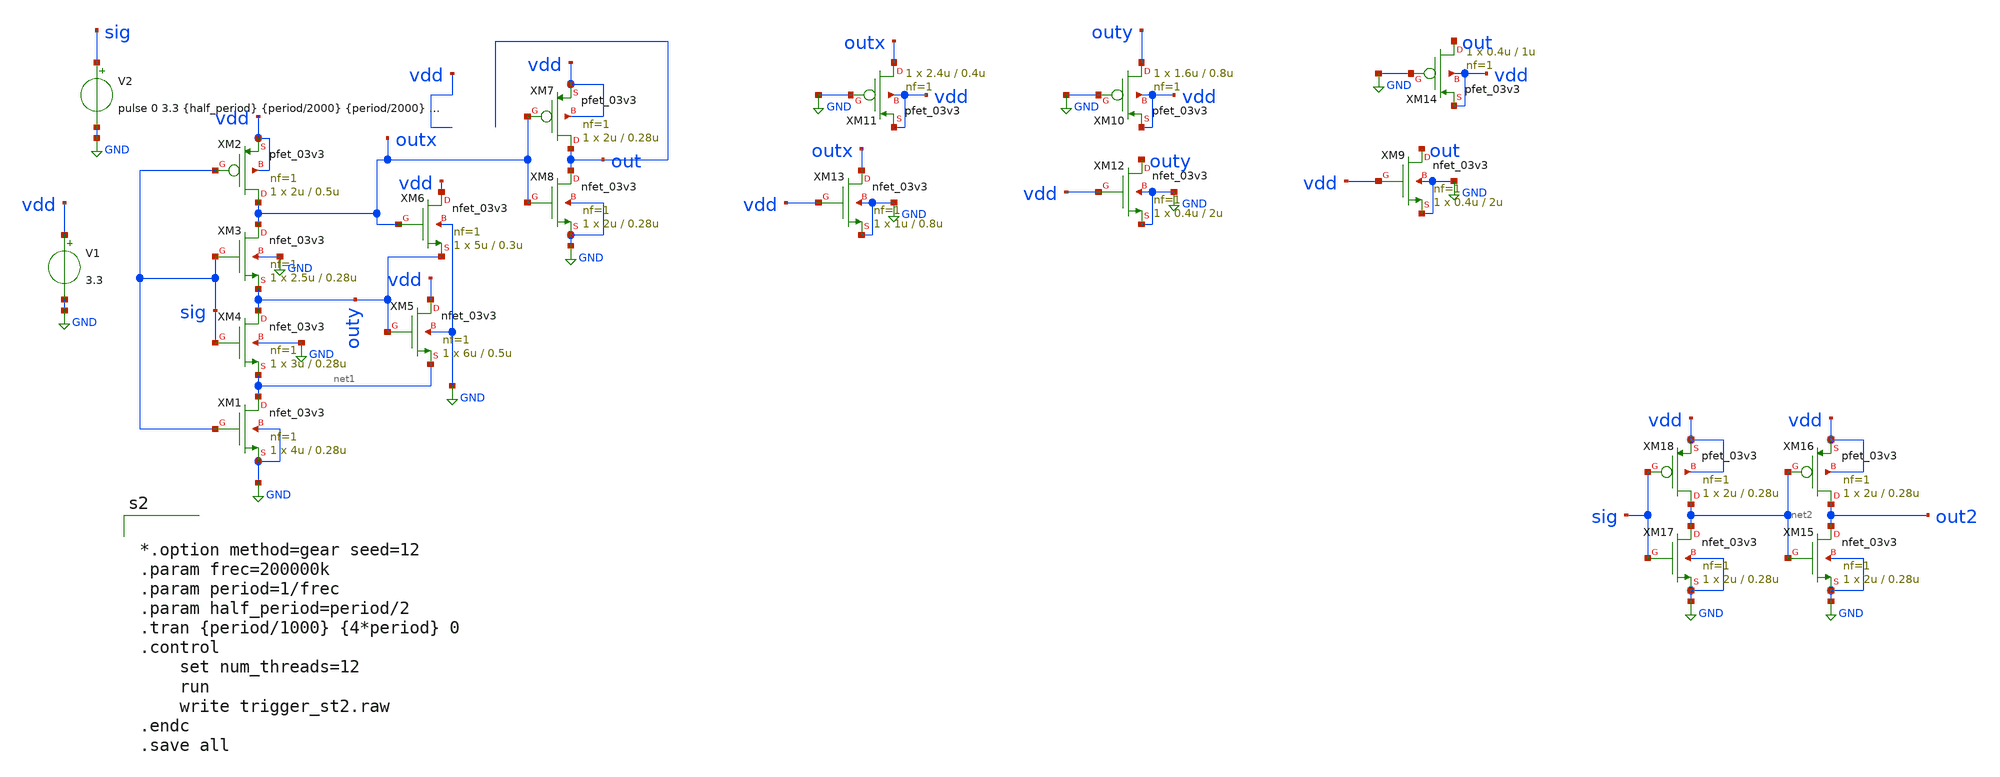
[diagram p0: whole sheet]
** sch_path: designs/libs/tb_trigger/trigger_st2.sch
**.subckt trigger_st2
XM2 outx sig vdd vdd pfet_03v3 L=0.5u W=2u nf=1 ad='int((nf+1)/2) * W/nf * 0.18u' as='int((nf+2)/2) * W/nf * 0.18u'
+ pd='2*int((nf+1)/2) * (W/nf + 0.18u)' ps='2*int((nf+2)/2) * (W/nf + 0.18u)' nrd='0.18u / W' nrs='0.18u / W'
+ sa=0 sb=0 sd=0 m=1
V2 sig GND pulse 0 3.3 {half_period} {period/2000} {period/2000} {half_period} {period}
V1 vdd GND 3.3
XM1 net1 sig GND GND nfet_03v3 L=0.28u W=4u nf=1 ad='int((nf+1)/2) * W/nf * 0.18u' as='int((nf+2)/2) * W/nf * 0.18u'
+ pd='2*int((nf+1)/2) * (W/nf + 0.18u)' ps='2*int((nf+2)/2) * (W/nf + 0.18u)' nrd='0.18u / W' nrs='0.18u / W'
+ sa=0 sb=0 sd=0 m=1
XM4 outy sig net1 GND nfet_03v3 L=0.28u W=3u nf=1 ad='int((nf+1)/2) * W/nf * 0.18u' as='int((nf+2)/2) * W/nf * 0.18u'
+ pd='2*int((nf+1)/2) * (W/nf + 0.18u)' ps='2*int((nf+2)/2) * (W/nf + 0.18u)' nrd='0.18u / W' nrs='0.18u / W'
+ sa=0 sb=0 sd=0 m=1
XM3 outx sig outy GND nfet_03v3 L=0.28u W=2.5u nf=1 ad='int((nf+1)/2) * W/nf * 0.18u' as='int((nf+2)/2) * W/nf * 0.18u'
+ pd='2*int((nf+1)/2) * (W/nf + 0.18u)' ps='2*int((nf+2)/2) * (W/nf + 0.18u)' nrd='0.18u / W' nrs='0.18u / W'
+ sa=0 sb=0 sd=0 m=1
XM5 vdd outy net1 GND nfet_03v3 L=0.5u W=6u nf=1 ad='int((nf+1)/2) * W/nf * 0.18u' as='int((nf+2)/2) * W/nf * 0.18u'
+ pd='2*int((nf+1)/2) * (W/nf + 0.18u)' ps='2*int((nf+2)/2) * (W/nf + 0.18u)' nrd='0.18u / W' nrs='0.18u / W'
+ sa=0 sb=0 sd=0 m=1
XM6 vdd outx outy GND nfet_03v3 L=0.3u W=5u nf=1 ad='int((nf+1)/2) * W/nf * 0.18u' as='int((nf+2)/2) * W/nf * 0.18u'
+ pd='2*int((nf+1)/2) * (W/nf + 0.18u)' ps='2*int((nf+2)/2) * (W/nf + 0.18u)' nrd='0.18u / W' nrs='0.18u / W'
+ sa=0 sb=0 sd=0 m=1
XM8 out outx GND GND nfet_03v3 L=0.28u W=2u nf=1 ad='int((nf+1)/2) * W/nf * 0.18u' as='int((nf+2)/2) * W/nf * 0.18u'
+ pd='2*int((nf+1)/2) * (W/nf + 0.18u)' ps='2*int((nf+2)/2) * (W/nf + 0.18u)' nrd='0.18u / W' nrs='0.18u / W'
+ sa=0 sb=0 sd=0 m=1
XM7 out outx vdd vdd pfet_03v3 L=0.28u W=2u nf=1 ad='int((nf+1)/2) * W/nf * 0.18u' as='int((nf+2)/2) * W/nf * 0.18u'
+ pd='2*int((nf+1)/2) * (W/nf + 0.18u)' ps='2*int((nf+2)/2) * (W/nf + 0.18u)' nrd='0.18u / W' nrs='0.18u / W'
+ sa=0 sb=0 sd=0 m=1
XM9 out vdd GND GND nfet_03v3 L=2u W=0.4u nf=1 ad='int((nf+1)/2) * W/nf * 0.18u' as='int((nf+2)/2) * W/nf * 0.18u'
+ pd='2*int((nf+1)/2) * (W/nf + 0.18u)' ps='2*int((nf+2)/2) * (W/nf + 0.18u)' nrd='0.18u / W' nrs='0.18u / W'
+ sa=0 sb=0 sd=0 m=1
XM14 out GND vdd vdd pfet_03v3 L=1u W=0.4u nf=1 ad='int((nf+1)/2) * W/nf * 0.18u' as='int((nf+2)/2) * W/nf * 0.18u'
+ pd='2*int((nf+1)/2) * (W/nf + 0.18u)' ps='2*int((nf+2)/2) * (W/nf + 0.18u)' nrd='0.18u / W' nrs='0.18u / W'
+ sa=0 sb=0 sd=0 m=1
XM10 outy GND vdd vdd pfet_03v3 L=0.8u W=1.6u nf=1 ad='int((nf+1)/2) * W/nf * 0.18u' as='int((nf+2)/2) * W/nf * 0.18u'
+ pd='2*int((nf+1)/2) * (W/nf + 0.18u)' ps='2*int((nf+2)/2) * (W/nf + 0.18u)' nrd='0.18u / W' nrs='0.18u / W'
+ sa=0 sb=0 sd=0 m=1
XM11 outx GND vdd vdd pfet_03v3 L=0.4u W=2.4u nf=1 ad='int((nf+1)/2) * W/nf * 0.18u' as='int((nf+2)/2) * W/nf * 0.18u'
+ pd='2*int((nf+1)/2) * (W/nf + 0.18u)' ps='2*int((nf+2)/2) * (W/nf + 0.18u)' nrd='0.18u / W' nrs='0.18u / W'
+ sa=0 sb=0 sd=0 m=1
XM12 outy vdd GND GND nfet_03v3 L=2u W=0.4u nf=1 ad='int((nf+1)/2) * W/nf * 0.18u' as='int((nf+2)/2) * W/nf * 0.18u'
+ pd='2*int((nf+1)/2) * (W/nf + 0.18u)' ps='2*int((nf+2)/2) * (W/nf + 0.18u)' nrd='0.18u / W' nrs='0.18u / W'
+ sa=0 sb=0 sd=0 m=1
XM13 outx vdd GND GND nfet_03v3 L=0.8u W=1u nf=1 ad='int((nf+1)/2) * W/nf * 0.18u' as='int((nf+2)/2) * W/nf * 0.18u'
+ pd='2*int((nf+1)/2) * (W/nf + 0.18u)' ps='2*int((nf+2)/2) * (W/nf + 0.18u)' nrd='0.18u / W' nrs='0.18u / W'
+ sa=0 sb=0 sd=0 m=1
XM15 out2 net2 GND GND nfet_03v3 L=0.28u W=2u nf=1 ad='int((nf+1)/2) * W/nf * 0.18u' as='int((nf+2)/2) * W/nf * 0.18u'
+ pd='2*int((nf+1)/2) * (W/nf + 0.18u)' ps='2*int((nf+2)/2) * (W/nf + 0.18u)' nrd='0.18u / W' nrs='0.18u / W'
+ sa=0 sb=0 sd=0 m=1
XM16 out2 net2 vdd vdd pfet_03v3 L=0.28u W=2u nf=1 ad='int((nf+1)/2) * W/nf * 0.18u' as='int((nf+2)/2) * W/nf * 0.18u'
+ pd='2*int((nf+1)/2) * (W/nf + 0.18u)' ps='2*int((nf+2)/2) * (W/nf + 0.18u)' nrd='0.18u / W' nrs='0.18u / W'
+ sa=0 sb=0 sd=0 m=1
XM17 net2 sig GND GND nfet_03v3 L=0.28u W=2u nf=1 ad='int((nf+1)/2) * W/nf * 0.18u' as='int((nf+2)/2) * W/nf * 0.18u'
+ pd='2*int((nf+1)/2) * (W/nf + 0.18u)' ps='2*int((nf+2)/2) * (W/nf + 0.18u)' nrd='0.18u / W' nrs='0.18u / W'
+ sa=0 sb=0 sd=0 m=1
XM18 net2 sig vdd vdd pfet_03v3 L=0.28u W=2u nf=1 ad='int((nf+1)/2) * W/nf * 0.18u' as='int((nf+2)/2) * W/nf * 0.18u'
+ pd='2*int((nf+1)/2) * (W/nf + 0.18u)' ps='2*int((nf+2)/2) * (W/nf + 0.18u)' nrd='0.18u / W' nrs='0.18u / W'
+ sa=0 sb=0 sd=0 m=1
**** begin user architecture code

.include $::180MCU_MODELS/design.ngspice
.lib $::180MCU_MODELS/sm141064.ngspice typical
.lib $::180MCU_MODELS/sm141064.ngspice cap_mim
.lib $::180MCU_MODELS/sm141064.ngspice res_typical
.lib $::180MCU_MODELS/sm141064.ngspice moscap_typical
.lib $::180MCU_MODELS/sm141064.ngspice mimcap_typical
.include /foss/pdks/gf180mcuD/libs.ref/gf180mcu_fd_sc_mcu9t5v0/spice/gf180mcu_fd_sc_mcu9t5v0.spice



*.option method=gear seed=12
.param frec=200000k
.param period=1/frec
.param half_period=period/2
.tran {period/1000} {4*period} 0
.control
	set num_threads=12
	run
	write trigger_st2.raw
.endc
.save all


**** end user architecture code
**.ends
.GLOBAL GND
.end
